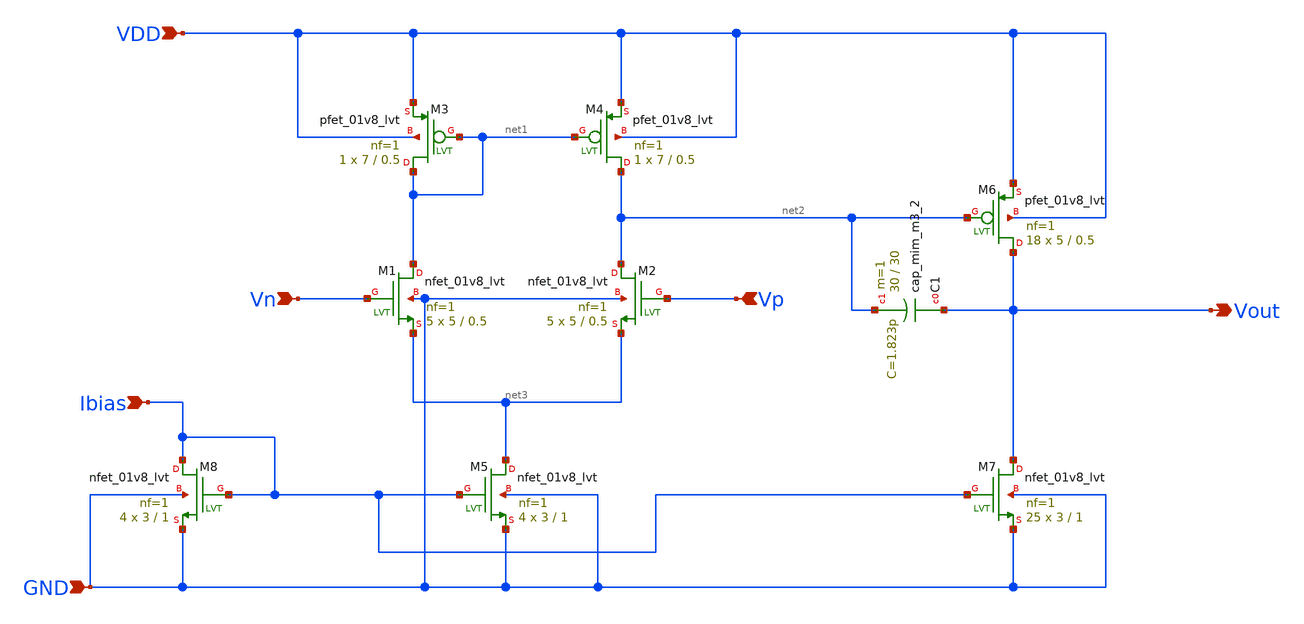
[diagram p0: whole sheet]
** sch_path: Analog_Blocks/OTA/Schematic/Miller_OTA/Transistor1.8v/Miller_OTA_NMOS_1.8v.sch
**.subckt Miller_OTA_NMOS_1.8v Ibias Vn Vp VDD GND Vout
*.ipin Ibias
*.ipin Vn
*.ipin Vp
*.ipin VDD
*.ipin GND
*.opin Vout
XM1 net1 Vn net3 GND sky130_fd_pr__nfet_01v8_lvt L=0.5 W=5 nf=1 ad='int((nf+1)/2) * W/nf * 0.29' as='int((nf+2)/2) * W/nf * 0.29'
+ pd='2*int((nf+1)/2) * (W/nf + 0.29)' ps='2*int((nf+2)/2) * (W/nf + 0.29)' nrd='0.29 / W' nrs='0.29 / W'
+ sa=0 sb=0 sd=0 mult=5 m=5
XM2 net2 Vp net3 GND sky130_fd_pr__nfet_01v8_lvt L=0.5 W=5 nf=1 ad='int((nf+1)/2) * W/nf * 0.29' as='int((nf+2)/2) * W/nf * 0.29'
+ pd='2*int((nf+1)/2) * (W/nf + 0.29)' ps='2*int((nf+2)/2) * (W/nf + 0.29)' nrd='0.29 / W' nrs='0.29 / W'
+ sa=0 sb=0 sd=0 mult=5 m=5
XM5 net3 Ibias GND GND sky130_fd_pr__nfet_01v8_lvt L=1 W=3 nf=1 ad='int((nf+1)/2) * W/nf * 0.29' as='int((nf+2)/2) * W/nf * 0.29'
+ pd='2*int((nf+1)/2) * (W/nf + 0.29)' ps='2*int((nf+2)/2) * (W/nf + 0.29)' nrd='0.29 / W' nrs='0.29 / W'
+ sa=0 sb=0 sd=0 mult=4 m=4
XM8 Ibias Ibias GND GND sky130_fd_pr__nfet_01v8_lvt L=1 W=3 nf=1 ad='int((nf+1)/2) * W/nf * 0.29' as='int((nf+2)/2) * W/nf * 0.29'
+ pd='2*int((nf+1)/2) * (W/nf + 0.29)' ps='2*int((nf+2)/2) * (W/nf + 0.29)' nrd='0.29 / W' nrs='0.29 / W'
+ sa=0 sb=0 sd=0 mult=4 m=4
XM7 Vout Ibias GND GND sky130_fd_pr__nfet_01v8_lvt L=1 W=3 nf=1 ad='int((nf+1)/2) * W/nf * 0.29' as='int((nf+2)/2) * W/nf * 0.29'
+ pd='2*int((nf+1)/2) * (W/nf + 0.29)' ps='2*int((nf+2)/2) * (W/nf + 0.29)' nrd='0.29 / W' nrs='0.29 / W'
+ sa=0 sb=0 sd=0 mult=25 m=25
XM4 net2 net1 VDD VDD sky130_fd_pr__pfet_01v8_lvt L=0.5 W=7 nf=1 ad='int((nf+1)/2) * W/nf * 0.29' as='int((nf+2)/2) * W/nf * 0.29'
+ pd='2*int((nf+1)/2) * (W/nf + 0.29)' ps='2*int((nf+2)/2) * (W/nf + 0.29)' nrd='0.29 / W' nrs='0.29 / W'
+ sa=0 sb=0 sd=0 mult=1 m=1
XM3 net1 net1 VDD VDD sky130_fd_pr__pfet_01v8_lvt L=0.5 W=7 nf=1 ad='int((nf+1)/2) * W/nf * 0.29' as='int((nf+2)/2) * W/nf * 0.29'
+ pd='2*int((nf+1)/2) * (W/nf + 0.29)' ps='2*int((nf+2)/2) * (W/nf + 0.29)' nrd='0.29 / W' nrs='0.29 / W'
+ sa=0 sb=0 sd=0 mult=1 m=1
XM6 Vout net2 VDD VDD sky130_fd_pr__pfet_01v8_lvt L=0.5 W=5 nf=1 ad='int((nf+1)/2) * W/nf * 0.29' as='int((nf+2)/2) * W/nf * 0.29'
+ pd='2*int((nf+1)/2) * (W/nf + 0.29)' ps='2*int((nf+2)/2) * (W/nf + 0.29)' nrd='0.29 / W' nrs='0.29 / W'
+ sa=0 sb=0 sd=0 mult=18 m=18
XC1 Vout net2 sky130_fd_pr__cap_mim_m3_2 W=30 L=30 MF=1 m=1
**.ends
.end
